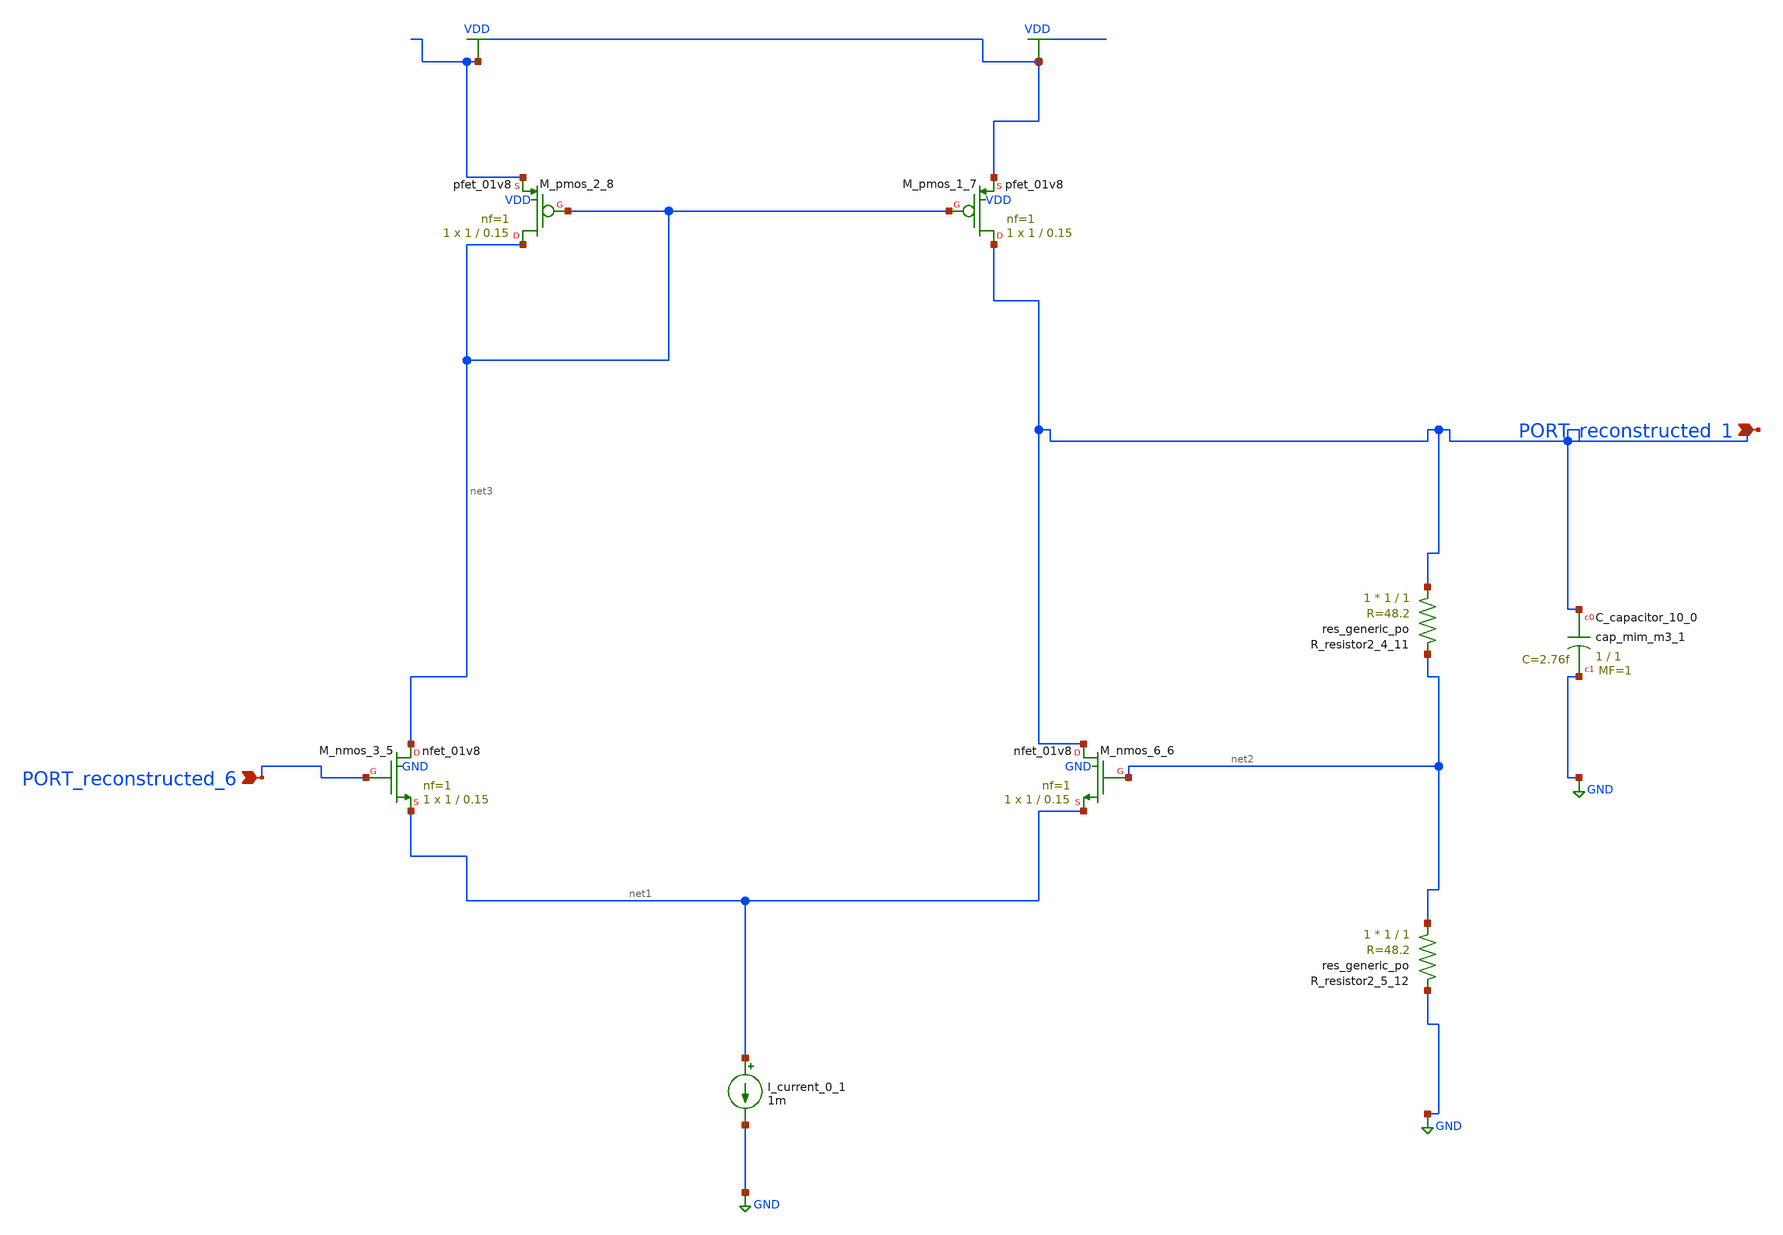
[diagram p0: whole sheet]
** sch_path: schematics/AMSNet/686.sch
**.subckt 686 PORT_reconstructed_1 PORT_reconstructed_6
*.ipin PORT_reconstructed_1
*.ipin PORT_reconstructed_6
XC_capacitor_10_0 PORT_reconstructed_1 GND sky130_fd_pr__cap_mim_m3_1 W=1 L=1 MF=1 m=1
I_current_0_1 net1 GND 1m
XM_nmos_3_5 net3 PORT_reconstructed_6 net1 GND sky130_fd_pr__nfet_01v8 L=0.15 W=1 nf=1 ad='int((1 + 1)/2) * 1 / 1 * 0.29'
+ as='int((1 + 2)/2) * 1 / 1 * 0.29' pd='2*int((1 + 1)/2) * (1 / 1 + 0.29)' ps='2*int((1 + 2)/2) * (1 / 1 + 0.29)'
+ nrd='0.29 / 1 ' nrs='0.29 / 1 ' sa=0 sb=0 sd=0 mult=1 m=1
XM_nmos_6_6 PORT_reconstructed_1 net2 net1 GND sky130_fd_pr__nfet_01v8 L=0.15 W=1 nf=1 ad='int((1 + 1)/2) * 1 / 1 * 0.29'
+ as='int((1 + 2)/2) * 1 / 1 * 0.29' pd='2*int((1 + 1)/2) * (1 / 1 + 0.29)' ps='2*int((1 + 2)/2) * (1 / 1 + 0.29)'
+ nrd='0.29 / 1 ' nrs='0.29 / 1 ' sa=0 sb=0 sd=0 mult=1 m=1
XM_pmos_1_7 PORT_reconstructed_1 net3 VDD VDD sky130_fd_pr__pfet_01v8 L=0.15 W=1 nf=1 ad='int((1 + 1)/2) * 1 / 1 * 0.29'
+ as='int((1 + 2)/2) * 1 / 1 * 0.29' pd='2*int((1 + 1)/2) * (1 / 1 + 0.29)' ps='2*int((1 + 2)/2) * (1 / 1 + 0.29)'
+ nrd='0.29 / 1 ' nrs='0.29 / 1 ' sa=0 sb=0 sd=0 mult=1 m=1
XM_pmos_2_8 net3 net3 VDD VDD sky130_fd_pr__pfet_01v8 L=0.15 W=1 nf=1 ad='int((1 + 1)/2) * 1 / 1 * 0.29'
+ as='int((1 + 2)/2) * 1 / 1 * 0.29' pd='2*int((1 + 1)/2) * (1 / 1 + 0.29)' ps='2*int((1 + 2)/2) * (1 / 1 + 0.29)'
+ nrd='0.29 / 1 ' nrs='0.29 / 1 ' sa=0 sb=0 sd=0 mult=1 m=1
XR_resistor2_4_11 PORT_reconstructed_1 net2 sky130_fd_pr__res_generic_po W=1 L=1 m=1
XR_resistor2_5_12 net2 GND sky130_fd_pr__res_generic_po W=1 L=1 m=1
**.ends
.GLOBAL GND
.GLOBAL VDD
.end
